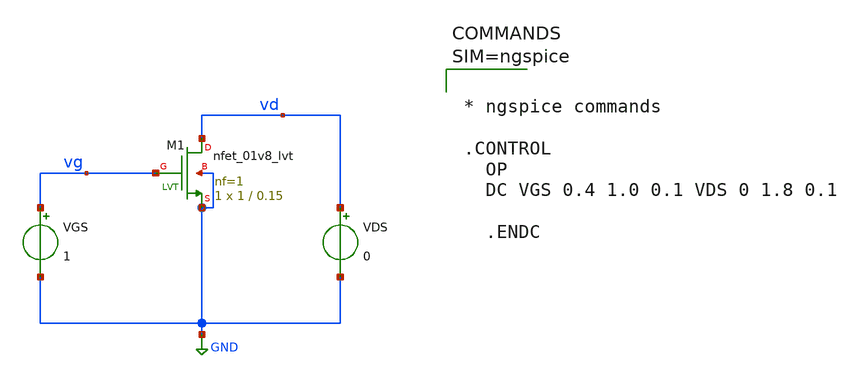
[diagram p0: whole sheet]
** sch_path: xschem/ID_VDS_NMOS.sch
**.subckt ID_VDS_NMOS
XM1 vd vg GND GND sky130_fd_pr__nfet_01v8_lvt L=0.15 W=1 nf=1 ad='int((1 + 1)/2) * 1 / 1 * 0.29' as='int((1 + 2)/2) * 1 / 1 * 0.29'
+ pd='2*int((1 + 1)/2) * (1 / 1 + 0.29)' ps='2*int((1 + 2)/2) * (1 / 1 + 0.29)' nrd='0.29 / 1 ' nrs='0.29 / 1 '
+ sa=0 sb=0 sd=0 mult=1 m=1
VGS vg GND 1
VDS vd GND 0
**** begin user architecture code



* ngspice commands

.CONTROL
  OP
  DC VGS 0.4 1.0 0.1 VDS 0 1.8 0.1

  .ENDC




** opencircuitdesign pdks install
.lib $::SKYWATER_MODELS/sky130.lib.spice tt

**** end user architecture code
**.ends
.GLOBAL GND
.end
